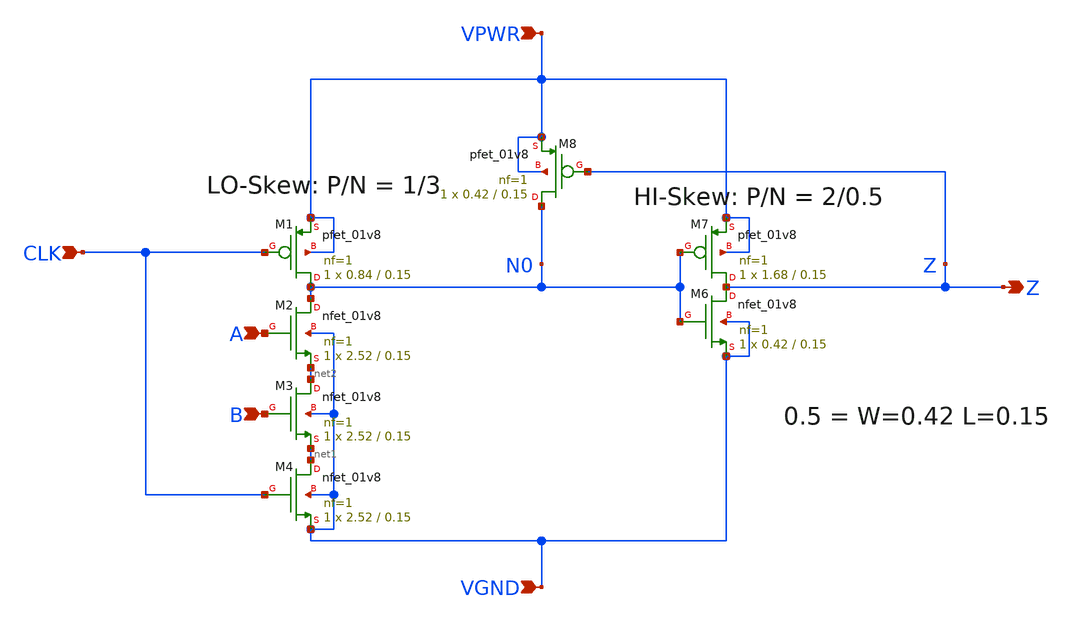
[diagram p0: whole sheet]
** sch_path: cells/xschem/sky130_lft_sc_dom__and2_1.sch
**.subckt sky130_lft_sc_dom__and2_1 A B CLK VPWR VGND Z
*.ipin A
*.ipin B
*.ipin CLK
*.ipin VPWR
*.ipin VGND
*.opin Z
XM1 N0 CLK VPWR VPWR sky130_fd_pr__pfet_01v8 L=0.15 W=0.84 nf=1 ad='int((1 + 1)/2) * 0.84 / 1 * 0.29'
+ as='int((1 + 2)/2) * 0.84 / 1 * 0.29' pd='2*int((1 + 1)/2) * (0.84 / 1 + 0.29)' ps='2*int((1 + 2)/2) * (0.84 / 1 + 0.29)'
+ nrd='0.29 / 0.84 ' nrs='0.29 / 0.84 ' sa=0 sb=0 sd=0 mult=1 m=1
XM2 N0 A net2 VGND sky130_fd_pr__nfet_01v8 L=0.15 W=2.52 nf=1 ad='int((1 + 1)/2) * 2.52 / 1 * 0.29' as='int((1 + 2)/2) * 2.52 / 1 * 0.29'
+ pd='2*int((1 + 1)/2) * (2.52 / 1 + 0.29)' ps='2*int((1 + 2)/2) * (2.52 / 1 + 0.29)' nrd='0.29 / 2.52 '
+ nrs='0.29 / 2.52 ' sa=0 sb=0 sd=0 mult=1 m=1
XM3 net2 B net1 VGND sky130_fd_pr__nfet_01v8 L=0.15 W=2.52 nf=1 ad='int((1 + 1)/2) * 2.52 / 1 * 0.29'
+ as='int((1 + 2)/2) * 2.52 / 1 * 0.29' pd='2*int((1 + 1)/2) * (2.52 / 1 + 0.29)' ps='2*int((1 + 2)/2) * (2.52 / 1 + 0.29)'
+ nrd='0.29 / 2.52 ' nrs='0.29 / 2.52 ' sa=0 sb=0 sd=0 mult=1 m=1
XM4 net1 CLK VGND VGND sky130_fd_pr__nfet_01v8 L=0.15 W=2.52 nf=1 ad='int((1 + 1)/2) * 2.52 / 1 * 0.29'
+ as='int((1 + 2)/2) * 2.52 / 1 * 0.29' pd='2*int((1 + 1)/2) * (2.52 / 1 + 0.29)' ps='2*int((1 + 2)/2) * (2.52 / 1 + 0.29)'
+ nrd='0.29 / 2.52 ' nrs='0.29 / 2.52 ' sa=0 sb=0 sd=0 mult=1 m=1
XM6 Z N0 VGND VGND sky130_fd_pr__nfet_01v8 L=0.15 W=0.42 nf=1 ad='int((1 + 1)/2) * 0.42 / 1 * 0.29' as='int((1 + 2)/2) * 0.42 / 1 * 0.29'
+ pd='2*int((1 + 1)/2) * (0.42 / 1 + 0.29)' ps='2*int((1 + 2)/2) * (0.42 / 1 + 0.29)' nrd='0.29 / 0.42 '
+ nrs='0.29 / 0.42 ' sa=0 sb=0 sd=0 mult=1 m=1
XM7 Z N0 VPWR VPWR sky130_fd_pr__pfet_01v8 L=0.15 W=1.68 nf=1 ad='int((1 + 1)/2) * 1.68 / 1 * 0.29' as='int((1 + 2)/2) * 1.68 / 1 * 0.29'
+ pd='2*int((1 + 1)/2) * (1.68 / 1 + 0.29)' ps='2*int((1 + 2)/2) * (1.68 / 1 + 0.29)' nrd='0.29 / 1.68 '
+ nrs='0.29 / 1.68 ' sa=0 sb=0 sd=0 mult=1 m=1
XM8 N0 Z VPWR VPWR sky130_fd_pr__pfet_01v8 L=0.15 W=0.42 nf=1 ad='int((1 + 1)/2) * 0.42 / 1 * 0.29' as='int((1 + 2)/2) * 0.42 / 1 * 0.29'
+ pd='2*int((1 + 1)/2) * (0.42 / 1 + 0.29)' ps='2*int((1 + 2)/2) * (0.42 / 1 + 0.29)' nrd='0.29 / 0.42 '
+ nrs='0.29 / 0.42 ' sa=0 sb=0 sd=0 mult=1 m=1
**.ends
.end
